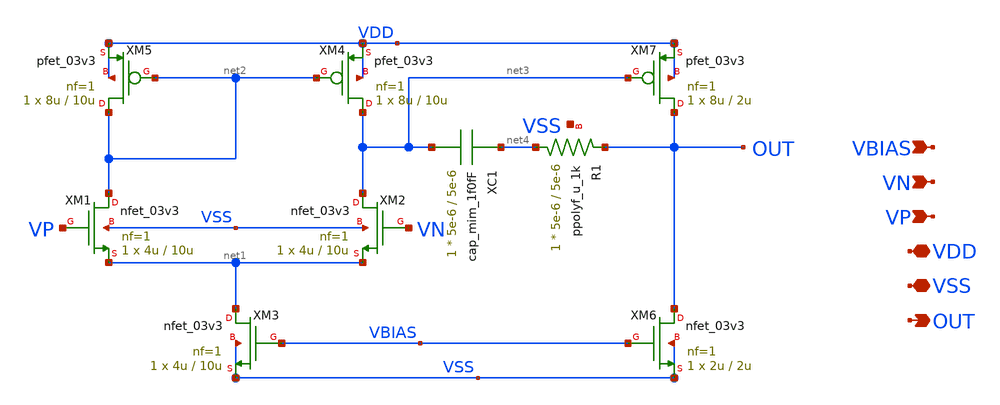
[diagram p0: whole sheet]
** sch_path: designs/libs/core_n-ota/nmos-ota/nmos-ota2.sch
**.subckt nmos-ota2 VN VP VDD VSS VBIAS OUT
*.ipin VN
*.ipin VP
*.iopin VDD
*.iopin VSS
*.ipin VBIAS
*.opin OUT
XM1 net2 VP net1 VSS nfet_03v3 L=10u W=4u nf=1 ad='int((nf+1)/2) * W/nf * 0.18u' as='int((nf+2)/2) * W/nf * 0.18u'
+ pd='2*int((nf+1)/2) * (W/nf + 0.18u)' ps='2*int((nf+2)/2) * (W/nf + 0.18u)' nrd='0.18u / W' nrs='0.18u / W'
+ sa=0 sb=0 sd=0 m=1
XM2 net3 VN net1 VSS nfet_03v3 L=10u W=4u nf=1 ad='int((nf+1)/2) * W/nf * 0.18u' as='int((nf+2)/2) * W/nf * 0.18u'
+ pd='2*int((nf+1)/2) * (W/nf + 0.18u)' ps='2*int((nf+2)/2) * (W/nf + 0.18u)' nrd='0.18u / W' nrs='0.18u / W'
+ sa=0 sb=0 sd=0 m=1
XM3 net1 VBIAS VSS VSS nfet_03v3 L=10u W=4u nf=1 ad='int((nf+1)/2) * W/nf * 0.18u' as='int((nf+2)/2) * W/nf * 0.18u'
+ pd='2*int((nf+1)/2) * (W/nf + 0.18u)' ps='2*int((nf+2)/2) * (W/nf + 0.18u)' nrd='0.18u / W' nrs='0.18u / W'
+ sa=0 sb=0 sd=0 m=1
XM4 net3 net2 VDD VDD pfet_03v3 L=10u W=8u nf=1 ad='int((nf+1)/2) * W/nf * 0.18u' as='int((nf+2)/2) * W/nf * 0.18u'
+ pd='2*int((nf+1)/2) * (W/nf + 0.18u)' ps='2*int((nf+2)/2) * (W/nf + 0.18u)' nrd='0.18u / W' nrs='0.18u / W'
+ sa=0 sb=0 sd=0 m=1
XM5 net2 net2 VDD VDD pfet_03v3 L=10u W=8u nf=1 ad='int((nf+1)/2) * W/nf * 0.18u' as='int((nf+2)/2) * W/nf * 0.18u'
+ pd='2*int((nf+1)/2) * (W/nf + 0.18u)' ps='2*int((nf+2)/2) * (W/nf + 0.18u)' nrd='0.18u / W' nrs='0.18u / W'
+ sa=0 sb=0 sd=0 m=1
XM6 OUT VBIAS VSS VSS nfet_03v3 L=2u W=2u nf=1 ad='int((nf+1)/2) * W/nf * 0.18u' as='int((nf+2)/2) * W/nf * 0.18u'
+ pd='2*int((nf+1)/2) * (W/nf + 0.18u)' ps='2*int((nf+2)/2) * (W/nf + 0.18u)' nrd='0.18u / W' nrs='0.18u / W'
+ sa=0 sb=0 sd=0 m=1
XC1 net4 net3 cap_mim_1f0fF c_width=5e-6 c_length=5e-6 m=1
XR1 net4 OUT VSS ppolyf_u_1k r_width=5e-6 r_length=5e-6 m=1
XM7 OUT net3 VDD VDD pfet_03v3 L=2u W=8u nf=1 ad='int((nf+1)/2) * W/nf * 0.18u' as='int((nf+2)/2) * W/nf * 0.18u'
+ pd='2*int((nf+1)/2) * (W/nf + 0.18u)' ps='2*int((nf+2)/2) * (W/nf + 0.18u)' nrd='0.18u / W' nrs='0.18u / W'
+ sa=0 sb=0 sd=0 m=1
**.ends
.end
